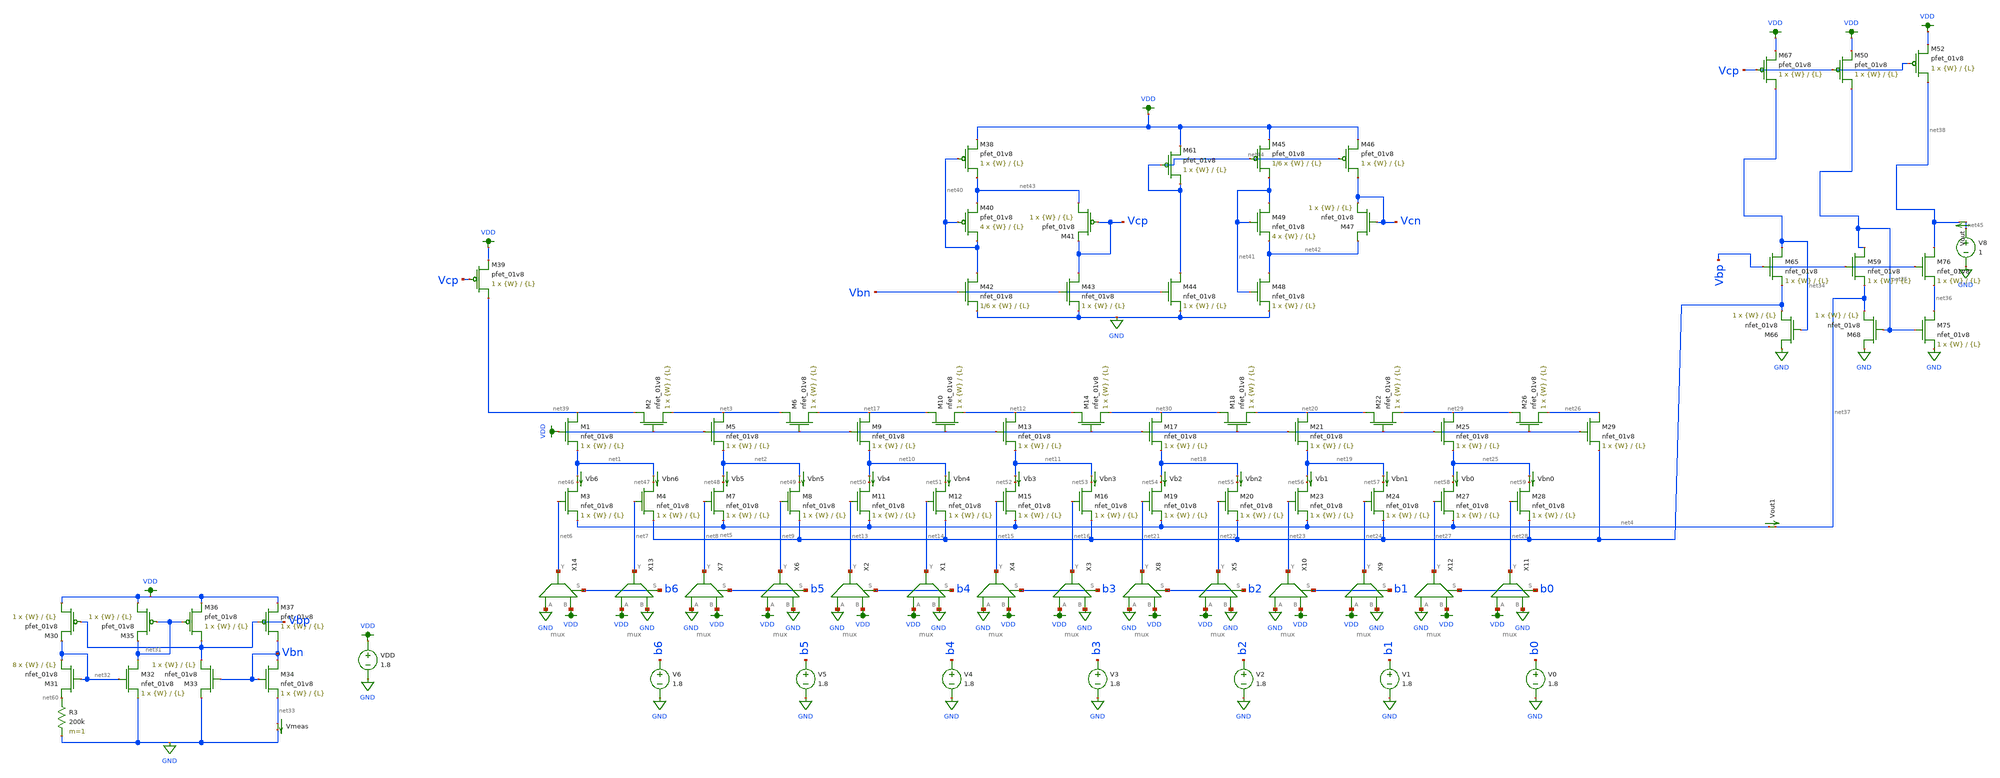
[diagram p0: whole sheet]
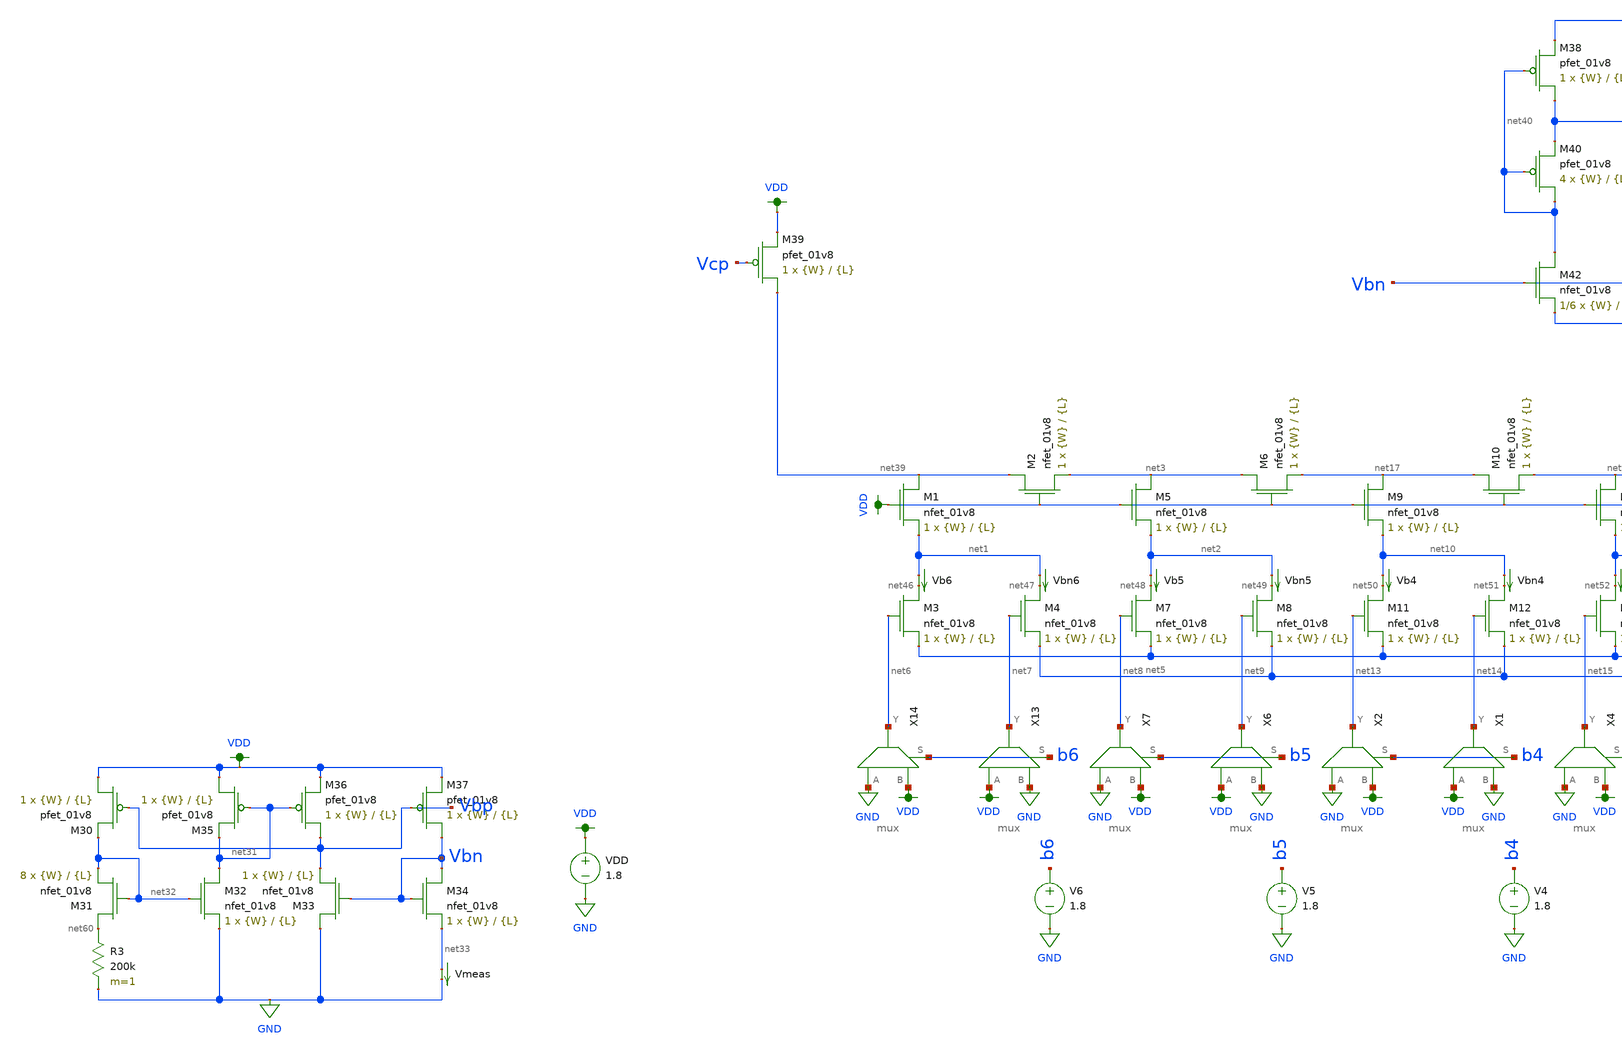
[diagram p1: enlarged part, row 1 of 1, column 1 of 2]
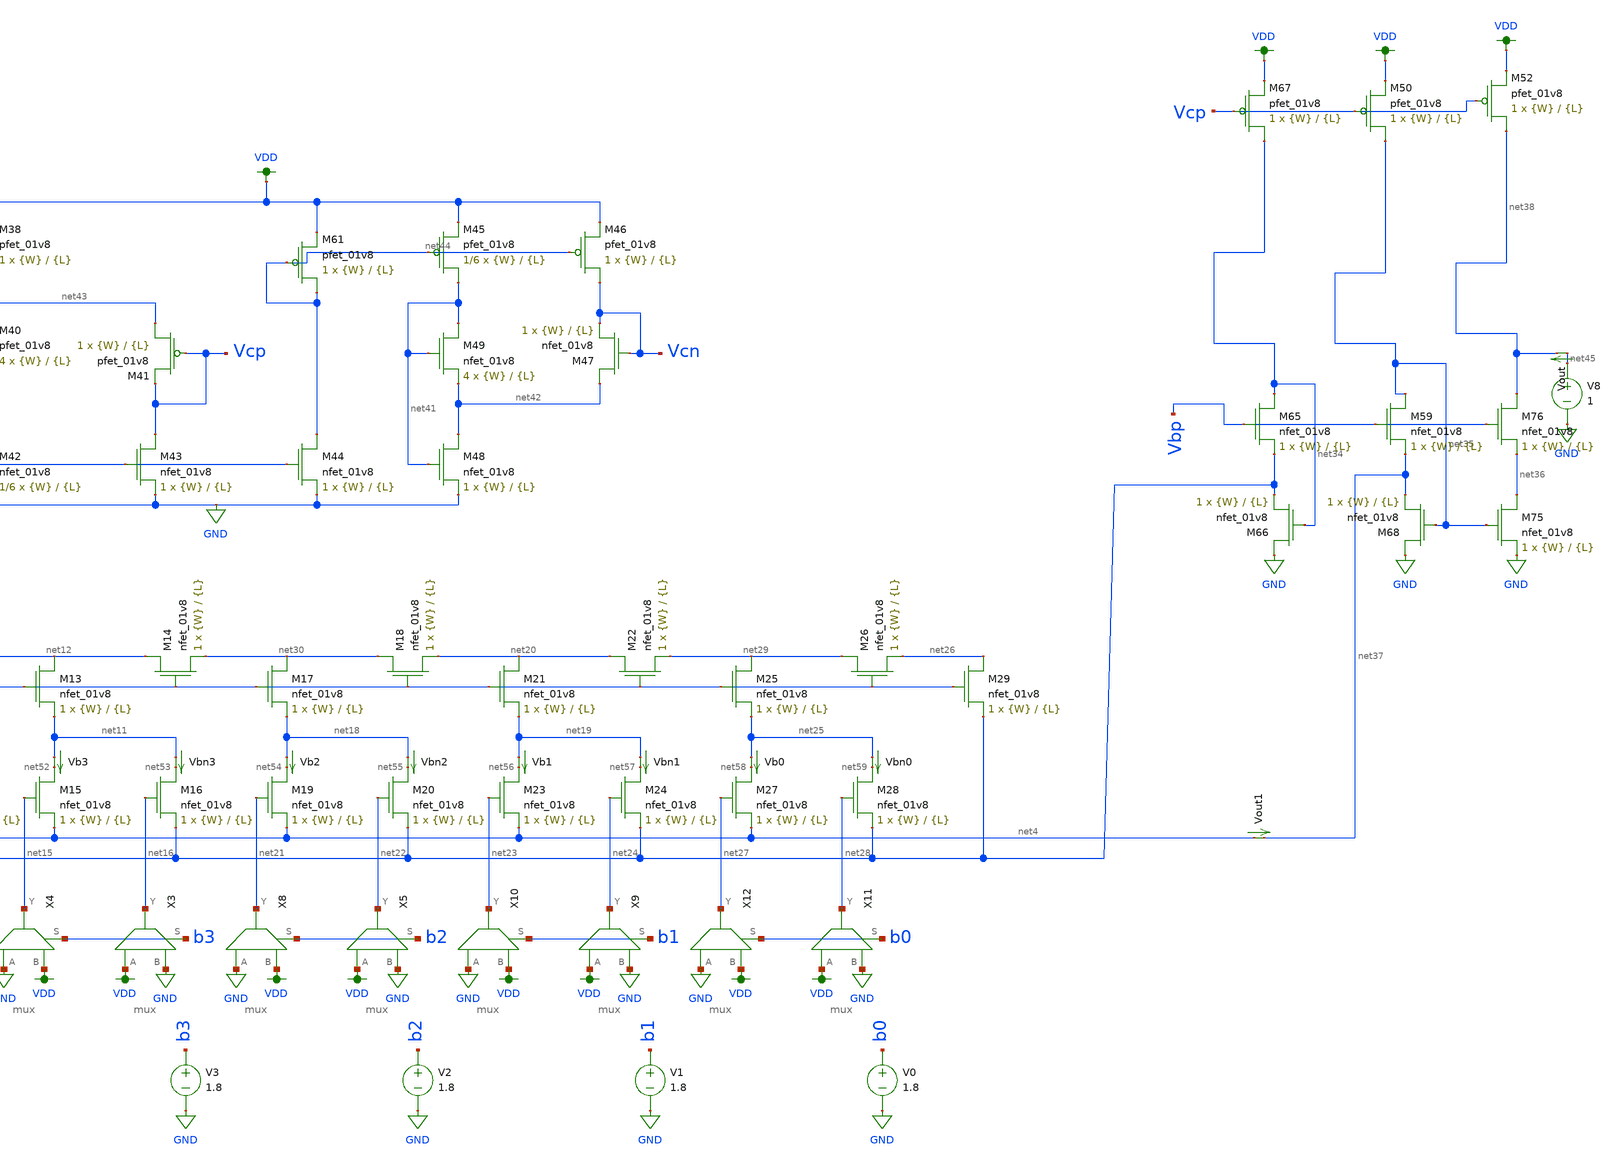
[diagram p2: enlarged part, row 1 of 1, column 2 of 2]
** sch_path: dac/schematics/misc/dac_from_paper_2.sch
**.subckt dac_from_paper_2
XM1 net39 VDD net1 GND sky130_fd_pr__nfet_01v8 L={L} W={W} nf=1 ad='int((nf+1)/2) * W/nf * 0.29' as='int((nf+2)/2) * W/nf * 0.29'
+ pd='2*int((nf+1)/2) * (W/nf + 0.29)' ps='2*int((nf+2)/2) * (W/nf + 0.29)' nrd='0.29 / W' nrs='0.29 / W'
+ sa=0 sb=0 sd=0 mult=1 m=1
XM2 net39 VDD net3 GND sky130_fd_pr__nfet_01v8 L={L} W={W} nf=1 ad='int((nf+1)/2) * W/nf * 0.29' as='int((nf+2)/2) * W/nf * 0.29'
+ pd='2*int((nf+1)/2) * (W/nf + 0.29)' ps='2*int((nf+2)/2) * (W/nf + 0.29)' nrd='0.29 / W' nrs='0.29 / W'
+ sa=0 sb=0 sd=0 mult=1 m=1
XM3 net46 net6 net4 GND sky130_fd_pr__nfet_01v8 L={L} W={W} nf=1 ad='int((nf+1)/2) * W/nf * 0.29' as='int((nf+2)/2) * W/nf * 0.29'
+ pd='2*int((nf+1)/2) * (W/nf + 0.29)' ps='2*int((nf+2)/2) * (W/nf + 0.29)' nrd='0.29 / W' nrs='0.29 / W'
+ sa=0 sb=0 sd=0 mult=1 m=1
XM4 net47 net7 net5 GND sky130_fd_pr__nfet_01v8 L={L} W={W} nf=1 ad='int((nf+1)/2) * W/nf * 0.29' as='int((nf+2)/2) * W/nf * 0.29'
+ pd='2*int((nf+1)/2) * (W/nf + 0.29)' ps='2*int((nf+2)/2) * (W/nf + 0.29)' nrd='0.29 / W' nrs='0.29 / W'
+ sa=0 sb=0 sd=0 mult=1 m=1
XM5 net3 VDD net2 GND sky130_fd_pr__nfet_01v8 L={L} W={W} nf=1 ad='int((nf+1)/2) * W/nf * 0.29' as='int((nf+2)/2) * W/nf * 0.29'
+ pd='2*int((nf+1)/2) * (W/nf + 0.29)' ps='2*int((nf+2)/2) * (W/nf + 0.29)' nrd='0.29 / W' nrs='0.29 / W'
+ sa=0 sb=0 sd=0 mult=1 m=1
XM6 net3 VDD net17 GND sky130_fd_pr__nfet_01v8 L={L} W={W} nf=1 ad='int((nf+1)/2) * W/nf * 0.29' as='int((nf+2)/2) * W/nf * 0.29'
+ pd='2*int((nf+1)/2) * (W/nf + 0.29)' ps='2*int((nf+2)/2) * (W/nf + 0.29)' nrd='0.29 / W' nrs='0.29 / W'
+ sa=0 sb=0 sd=0 mult=1 m=1
XM7 net48 net8 net4 GND sky130_fd_pr__nfet_01v8 L={L} W={W} nf=1 ad='int((nf+1)/2) * W/nf * 0.29' as='int((nf+2)/2) * W/nf * 0.29'
+ pd='2*int((nf+1)/2) * (W/nf + 0.29)' ps='2*int((nf+2)/2) * (W/nf + 0.29)' nrd='0.29 / W' nrs='0.29 / W'
+ sa=0 sb=0 sd=0 mult=1 m=1
XM8 net49 net9 net5 GND sky130_fd_pr__nfet_01v8 L={L} W={W} nf=1 ad='int((nf+1)/2) * W/nf * 0.29' as='int((nf+2)/2) * W/nf * 0.29'
+ pd='2*int((nf+1)/2) * (W/nf + 0.29)' ps='2*int((nf+2)/2) * (W/nf + 0.29)' nrd='0.29 / W' nrs='0.29 / W'
+ sa=0 sb=0 sd=0 mult=1 m=1
XM9 net17 VDD net10 GND sky130_fd_pr__nfet_01v8 L={L} W={W} nf=1 ad='int((nf+1)/2) * W/nf * 0.29' as='int((nf+2)/2) * W/nf * 0.29'
+ pd='2*int((nf+1)/2) * (W/nf + 0.29)' ps='2*int((nf+2)/2) * (W/nf + 0.29)' nrd='0.29 / W' nrs='0.29 / W'
+ sa=0 sb=0 sd=0 mult=1 m=1
XM10 net17 VDD net12 GND sky130_fd_pr__nfet_01v8 L={L} W={W} nf=1 ad='int((nf+1)/2) * W/nf * 0.29' as='int((nf+2)/2) * W/nf * 0.29'
+ pd='2*int((nf+1)/2) * (W/nf + 0.29)' ps='2*int((nf+2)/2) * (W/nf + 0.29)' nrd='0.29 / W' nrs='0.29 / W'
+ sa=0 sb=0 sd=0 mult=1 m=1
XM11 net50 net13 net4 GND sky130_fd_pr__nfet_01v8 L={L} W={W} nf=1 ad='int((nf+1)/2) * W/nf * 0.29' as='int((nf+2)/2) * W/nf * 0.29'
+ pd='2*int((nf+1)/2) * (W/nf + 0.29)' ps='2*int((nf+2)/2) * (W/nf + 0.29)' nrd='0.29 / W' nrs='0.29 / W'
+ sa=0 sb=0 sd=0 mult=1 m=1
XM12 net51 net14 net5 GND sky130_fd_pr__nfet_01v8 L={L} W={W} nf=1 ad='int((nf+1)/2) * W/nf * 0.29' as='int((nf+2)/2) * W/nf * 0.29'
+ pd='2*int((nf+1)/2) * (W/nf + 0.29)' ps='2*int((nf+2)/2) * (W/nf + 0.29)' nrd='0.29 / W' nrs='0.29 / W'
+ sa=0 sb=0 sd=0 mult=1 m=1
XM13 net12 VDD net11 GND sky130_fd_pr__nfet_01v8 L={L} W={W} nf=1 ad='int((nf+1)/2) * W/nf * 0.29' as='int((nf+2)/2) * W/nf * 0.29'
+ pd='2*int((nf+1)/2) * (W/nf + 0.29)' ps='2*int((nf+2)/2) * (W/nf + 0.29)' nrd='0.29 / W' nrs='0.29 / W'
+ sa=0 sb=0 sd=0 mult=1 m=1
XM14 net12 VDD net30 GND sky130_fd_pr__nfet_01v8 L={L} W={W} nf=1 ad='int((nf+1)/2) * W/nf * 0.29' as='int((nf+2)/2) * W/nf * 0.29'
+ pd='2*int((nf+1)/2) * (W/nf + 0.29)' ps='2*int((nf+2)/2) * (W/nf + 0.29)' nrd='0.29 / W' nrs='0.29 / W'
+ sa=0 sb=0 sd=0 mult=1 m=1
XM15 net52 net15 net4 GND sky130_fd_pr__nfet_01v8 L={L} W={W} nf=1 ad='int((nf+1)/2) * W/nf * 0.29' as='int((nf+2)/2) * W/nf * 0.29'
+ pd='2*int((nf+1)/2) * (W/nf + 0.29)' ps='2*int((nf+2)/2) * (W/nf + 0.29)' nrd='0.29 / W' nrs='0.29 / W'
+ sa=0 sb=0 sd=0 mult=1 m=1
XM16 net53 net16 net5 GND sky130_fd_pr__nfet_01v8 L={L} W={W} nf=1 ad='int((nf+1)/2) * W/nf * 0.29' as='int((nf+2)/2) * W/nf * 0.29'
+ pd='2*int((nf+1)/2) * (W/nf + 0.29)' ps='2*int((nf+2)/2) * (W/nf + 0.29)' nrd='0.29 / W' nrs='0.29 / W'
+ sa=0 sb=0 sd=0 mult=1 m=1
XM17 net30 VDD net18 GND sky130_fd_pr__nfet_01v8 L={L} W={W} nf=1 ad='int((nf+1)/2) * W/nf * 0.29' as='int((nf+2)/2) * W/nf * 0.29'
+ pd='2*int((nf+1)/2) * (W/nf + 0.29)' ps='2*int((nf+2)/2) * (W/nf + 0.29)' nrd='0.29 / W' nrs='0.29 / W'
+ sa=0 sb=0 sd=0 mult=1 m=1
XM18 net30 VDD net20 GND sky130_fd_pr__nfet_01v8 L={L} W={W} nf=1 ad='int((nf+1)/2) * W/nf * 0.29' as='int((nf+2)/2) * W/nf * 0.29'
+ pd='2*int((nf+1)/2) * (W/nf + 0.29)' ps='2*int((nf+2)/2) * (W/nf + 0.29)' nrd='0.29 / W' nrs='0.29 / W'
+ sa=0 sb=0 sd=0 mult=1 m=1
XM19 net54 net21 net4 GND sky130_fd_pr__nfet_01v8 L={L} W={W} nf=1 ad='int((nf+1)/2) * W/nf * 0.29' as='int((nf+2)/2) * W/nf * 0.29'
+ pd='2*int((nf+1)/2) * (W/nf + 0.29)' ps='2*int((nf+2)/2) * (W/nf + 0.29)' nrd='0.29 / W' nrs='0.29 / W'
+ sa=0 sb=0 sd=0 mult=1 m=1
XM20 net55 net22 net5 GND sky130_fd_pr__nfet_01v8 L={L} W={W} nf=1 ad='int((nf+1)/2) * W/nf * 0.29' as='int((nf+2)/2) * W/nf * 0.29'
+ pd='2*int((nf+1)/2) * (W/nf + 0.29)' ps='2*int((nf+2)/2) * (W/nf + 0.29)' nrd='0.29 / W' nrs='0.29 / W'
+ sa=0 sb=0 sd=0 mult=1 m=1
XM21 net20 VDD net19 GND sky130_fd_pr__nfet_01v8 L={L} W={W} nf=1 ad='int((nf+1)/2) * W/nf * 0.29' as='int((nf+2)/2) * W/nf * 0.29'
+ pd='2*int((nf+1)/2) * (W/nf + 0.29)' ps='2*int((nf+2)/2) * (W/nf + 0.29)' nrd='0.29 / W' nrs='0.29 / W'
+ sa=0 sb=0 sd=0 mult=1 m=1
XM22 net20 VDD net29 GND sky130_fd_pr__nfet_01v8 L={L} W={W} nf=1 ad='int((nf+1)/2) * W/nf * 0.29' as='int((nf+2)/2) * W/nf * 0.29'
+ pd='2*int((nf+1)/2) * (W/nf + 0.29)' ps='2*int((nf+2)/2) * (W/nf + 0.29)' nrd='0.29 / W' nrs='0.29 / W'
+ sa=0 sb=0 sd=0 mult=1 m=1
XM23 net56 net23 net4 GND sky130_fd_pr__nfet_01v8 L={L} W={W} nf=1 ad='int((nf+1)/2) * W/nf * 0.29' as='int((nf+2)/2) * W/nf * 0.29'
+ pd='2*int((nf+1)/2) * (W/nf + 0.29)' ps='2*int((nf+2)/2) * (W/nf + 0.29)' nrd='0.29 / W' nrs='0.29 / W'
+ sa=0 sb=0 sd=0 mult=1 m=1
XM24 net57 net24 net5 GND sky130_fd_pr__nfet_01v8 L={L} W={W} nf=1 ad='int((nf+1)/2) * W/nf * 0.29' as='int((nf+2)/2) * W/nf * 0.29'
+ pd='2*int((nf+1)/2) * (W/nf + 0.29)' ps='2*int((nf+2)/2) * (W/nf + 0.29)' nrd='0.29 / W' nrs='0.29 / W'
+ sa=0 sb=0 sd=0 mult=1 m=1
XM25 net29 VDD net25 GND sky130_fd_pr__nfet_01v8 L={L} W={W} nf=1 ad='int((nf+1)/2) * W/nf * 0.29' as='int((nf+2)/2) * W/nf * 0.29'
+ pd='2*int((nf+1)/2) * (W/nf + 0.29)' ps='2*int((nf+2)/2) * (W/nf + 0.29)' nrd='0.29 / W' nrs='0.29 / W'
+ sa=0 sb=0 sd=0 mult=1 m=1
XM26 net29 VDD net26 GND sky130_fd_pr__nfet_01v8 L={L} W={W} nf=1 ad='int((nf+1)/2) * W/nf * 0.29' as='int((nf+2)/2) * W/nf * 0.29'
+ pd='2*int((nf+1)/2) * (W/nf + 0.29)' ps='2*int((nf+2)/2) * (W/nf + 0.29)' nrd='0.29 / W' nrs='0.29 / W'
+ sa=0 sb=0 sd=0 mult=1 m=1
XM27 net58 net27 net4 GND sky130_fd_pr__nfet_01v8 L={L} W={W} nf=1 ad='int((nf+1)/2) * W/nf * 0.29' as='int((nf+2)/2) * W/nf * 0.29'
+ pd='2*int((nf+1)/2) * (W/nf + 0.29)' ps='2*int((nf+2)/2) * (W/nf + 0.29)' nrd='0.29 / W' nrs='0.29 / W'
+ sa=0 sb=0 sd=0 mult=1 m=1
XM28 net59 net28 net5 GND sky130_fd_pr__nfet_01v8 L={L} W={W} nf=1 ad='int((nf+1)/2) * W/nf * 0.29' as='int((nf+2)/2) * W/nf * 0.29'
+ pd='2*int((nf+1)/2) * (W/nf + 0.29)' ps='2*int((nf+2)/2) * (W/nf + 0.29)' nrd='0.29 / W' nrs='0.29 / W'
+ sa=0 sb=0 sd=0 mult=1 m=1
XM29 net26 VDD net5 GND sky130_fd_pr__nfet_01v8 L={L} W={W} nf=1 ad='int((nf+1)/2) * W/nf * 0.29' as='int((nf+2)/2) * W/nf * 0.29'
+ pd='2*int((nf+1)/2) * (W/nf + 0.29)' ps='2*int((nf+2)/2) * (W/nf + 0.29)' nrd='0.29 / W' nrs='0.29 / W'
+ sa=0 sb=0 sd=0 mult=1 m=1
Vb0 net25 net58 0
.save i(vb0)
Vbn0 net25 net59 0
.save i(vbn0)
Vb5 net2 net48 0
.save i(vb5)
Vb6 net1 net46 0
.save i(vb6)
Vb1 net19 net56 0
.save i(vb1)
Vb2 net18 net54 0
.save i(vb2)
Vb3 net11 net52 0
.save i(vb3)
Vb4 net10 net50 0
.save i(vb4)
Vbn1 net19 net57 0
.save i(vbn1)
Vbn2 net18 net55 0
.save i(vbn2)
Vbn3 net11 net53 0
.save i(vbn3)
Vbn4 net10 net51 0
.save i(vbn4)
Vbn5 net2 net49 0
.save i(vbn5)
Vbn6 net1 net47 0
.save i(vbn6)
V0 b0 GND 1.8
V1 b1 GND 1.8
V2 b2 GND 1.8
V3 b3 GND 1.8
V4 b4 GND 1.8
V5 b5 GND 1.8
V6 b6 GND 1.8
XM30 VDD Vbp net32 VDD sky130_fd_pr__pfet_01v8 L={L} W={W} nf=1 ad='int((nf+1)/2) * W/nf * 0.29' as='int((nf+2)/2) * W/nf * 0.29'
+ pd='2*int((nf+1)/2) * (W/nf + 0.29)' ps='2*int((nf+2)/2) * (W/nf + 0.29)' nrd='0.29 / W' nrs='0.29 / W'
+ sa=0 sb=0 sd=0 mult=1 m=1
XM31 net60 net32 net32 GND sky130_fd_pr__nfet_01v8 L={L} W={W} nf=1 ad='int((nf+1)/2) * W/nf * 0.29'
+ as='int((nf+2)/2) * W/nf * 0.29' pd='2*int((nf+1)/2) * (W/nf + 0.29)' ps='2*int((nf+2)/2) * (W/nf + 0.29)'
+ nrd='0.29 / W' nrs='0.29 / W' sa=0 sb=0 sd=0 mult=8 m=8
R3 net60 GND 200k m=1
XM32 net31 net32 GND GND sky130_fd_pr__nfet_01v8 L={L} W={W} nf=1 ad='int((nf+1)/2) * W/nf * 0.29' as='int((nf+2)/2) * W/nf * 0.29'
+ pd='2*int((nf+1)/2) * (W/nf + 0.29)' ps='2*int((nf+2)/2) * (W/nf + 0.29)' nrd='0.29 / W' nrs='0.29 / W'
+ sa=0 sb=0 sd=0 mult=1 m=1
XM33 GND Vbn Vbp GND sky130_fd_pr__nfet_01v8 L={L} W={W} nf=1 ad='int((nf+1)/2) * W/nf * 0.29' as='int((nf+2)/2) * W/nf * 0.29'
+ pd='2*int((nf+1)/2) * (W/nf + 0.29)' ps='2*int((nf+2)/2) * (W/nf + 0.29)' nrd='0.29 / W' nrs='0.29 / W'
+ sa=0 sb=0 sd=0 mult=1 m=1
XM34 Vbn Vbn net33 GND sky130_fd_pr__nfet_01v8 L={L} W={W} nf=1 ad='int((nf+1)/2) * W/nf * 0.29' as='int((nf+2)/2) * W/nf * 0.29'
+ pd='2*int((nf+1)/2) * (W/nf + 0.29)' ps='2*int((nf+2)/2) * (W/nf + 0.29)' nrd='0.29 / W' nrs='0.29 / W'
+ sa=0 sb=0 sd=0 mult=1 m=1
XM35 VDD net31 net31 VDD sky130_fd_pr__pfet_01v8 L={L} W={W} nf=1 ad='int((nf+1)/2) * W/nf * 0.29' as='int((nf+2)/2) * W/nf * 0.29'
+ pd='2*int((nf+1)/2) * (W/nf + 0.29)' ps='2*int((nf+2)/2) * (W/nf + 0.29)' nrd='0.29 / W' nrs='0.29 / W'
+ sa=0 sb=0 sd=0 mult=1 m=1
XM36 Vbp net31 VDD VDD sky130_fd_pr__pfet_01v8 L={L} W={W} nf=1 ad='int((nf+1)/2) * W/nf * 0.29' as='int((nf+2)/2) * W/nf * 0.29'
+ pd='2*int((nf+1)/2) * (W/nf + 0.29)' ps='2*int((nf+2)/2) * (W/nf + 0.29)' nrd='0.29 / W' nrs='0.29 / W'
+ sa=0 sb=0 sd=0 mult=1 m=1
XM37 Vbn Vbp VDD VDD sky130_fd_pr__pfet_01v8 L={L} W={W} nf=1 ad='int((nf+1)/2) * W/nf * 0.29' as='int((nf+2)/2) * W/nf * 0.29'
+ pd='2*int((nf+1)/2) * (W/nf + 0.29)' ps='2*int((nf+2)/2) * (W/nf + 0.29)' nrd='0.29 / W' nrs='0.29 / W'
+ sa=0 sb=0 sd=0 mult=1 m=1
VDD VDD GND 1.8
Vmeas net33 GND 0
.save i(vmeas)
X13 VDD GND net7 b6 mux
X14 GND VDD net6 b6 mux
X6 VDD GND net9 b5 mux
X7 GND VDD net8 b5 mux
X1 VDD GND net14 b4 mux
X2 GND VDD net13 b4 mux
X3 VDD GND net16 b3 mux
X4 GND VDD net15 b3 mux
X5 VDD GND net22 b2 mux
X8 GND VDD net21 b2 mux
X9 VDD GND net24 b1 mux
X10 GND VDD net23 b1 mux
X11 VDD GND net28 b0 mux
X12 GND VDD net27 b0 mux
XM65 net34 Vbp net5 GND sky130_fd_pr__nfet_01v8 L={L} W={W} nf=1 ad='int((nf+1)/2) * W/nf * 0.29' as='int((nf+2)/2) * W/nf * 0.29'
+ pd='2*int((nf+1)/2) * (W/nf + 0.29)' ps='2*int((nf+2)/2) * (W/nf + 0.29)' nrd='0.29 / W' nrs='0.29 / W'
+ sa=0 sb=0 sd=0 mult=1 m=1
XM66 GND net34 net5 GND sky130_fd_pr__nfet_01v8 L={L} W={W} nf=1 ad='int((nf+1)/2) * W/nf * 0.29' as='int((nf+2)/2) * W/nf * 0.29'
+ pd='2*int((nf+1)/2) * (W/nf + 0.29)' ps='2*int((nf+2)/2) * (W/nf + 0.29)' nrd='0.29 / W' nrs='0.29 / W'
+ sa=0 sb=0 sd=0 mult=1 m=1
XM59 net35 Vbp net37 GND sky130_fd_pr__nfet_01v8 L={L} W={W} nf=1 ad='int((nf+1)/2) * W/nf * 0.29' as='int((nf+2)/2) * W/nf * 0.29'
+ pd='2*int((nf+1)/2) * (W/nf + 0.29)' ps='2*int((nf+2)/2) * (W/nf + 0.29)' nrd='0.29 / W' nrs='0.29 / W'
+ sa=0 sb=0 sd=0 mult=1 m=1
XM68 GND net35 net37 GND sky130_fd_pr__nfet_01v8 L={L} W={W} nf=1 ad='int((nf+1)/2) * W/nf * 0.29' as='int((nf+2)/2) * W/nf * 0.29'
+ pd='2*int((nf+1)/2) * (W/nf + 0.29)' ps='2*int((nf+2)/2) * (W/nf + 0.29)' nrd='0.29 / W' nrs='0.29 / W'
+ sa=0 sb=0 sd=0 mult=1 m=1
XM75 net36 net35 GND GND sky130_fd_pr__nfet_01v8 L={L} W={W} nf=1 ad='int((nf+1)/2) * W/nf * 0.29' as='int((nf+2)/2) * W/nf * 0.29'
+ pd='2*int((nf+1)/2) * (W/nf + 0.29)' ps='2*int((nf+2)/2) * (W/nf + 0.29)' nrd='0.29 / W' nrs='0.29 / W'
+ sa=0 sb=0 sd=0 mult=1 m=1
XM76 net38 Vbp net36 GND sky130_fd_pr__nfet_01v8 L={L} W={W} nf=1 ad='int((nf+1)/2) * W/nf * 0.29' as='int((nf+2)/2) * W/nf * 0.29'
+ pd='2*int((nf+1)/2) * (W/nf + 0.29)' ps='2*int((nf+2)/2) * (W/nf + 0.29)' nrd='0.29 / W' nrs='0.29 / W'
+ sa=0 sb=0 sd=0 mult=1 m=1
Vout net45 net38 0
.save i(vout)
XM67 net34 Vcp VDD VDD sky130_fd_pr__pfet_01v8 L={L} W={W} nf=6 ad='int((nf+1)/2) * W/nf * 0.29' as='int((nf+2)/2) * W/nf * 0.29'
+ pd='2*int((nf+1)/2) * (W/nf + 0.29)' ps='2*int((nf+2)/2) * (W/nf + 0.29)' nrd='0.29 / W' nrs='0.29 / W'
+ sa=0 sb=0 sd=0 mult=1 m=1
XM50 net35 Vcp VDD VDD sky130_fd_pr__pfet_01v8 L={L} W={W} nf=6 ad='int((nf+1)/2) * W/nf * 0.29' as='int((nf+2)/2) * W/nf * 0.29'
+ pd='2*int((nf+1)/2) * (W/nf + 0.29)' ps='2*int((nf+2)/2) * (W/nf + 0.29)' nrd='0.29 / W' nrs='0.29 / W'
+ sa=0 sb=0 sd=0 mult=1 m=1
XM52 net38 Vcp VDD VDD sky130_fd_pr__pfet_01v8 L={L} W={W} nf=6 ad='int((nf+1)/2) * W/nf * 0.29' as='int((nf+2)/2) * W/nf * 0.29'
+ pd='2*int((nf+1)/2) * (W/nf + 0.29)' ps='2*int((nf+2)/2) * (W/nf + 0.29)' nrd='0.29 / W' nrs='0.29 / W'
+ sa=0 sb=0 sd=0 mult=1 m=1
Vout1 net4 net37 0
.save i(vout1)
XM39 net39 Vcp VDD VDD sky130_fd_pr__pfet_01v8 L={L} W={W} nf=1 ad='int((nf+1)/2) * W/nf * 0.29' as='int((nf+2)/2) * W/nf * 0.29'
+ pd='2*int((nf+1)/2) * (W/nf + 0.29)' ps='2*int((nf+2)/2) * (W/nf + 0.29)' nrd='0.29 / W' nrs='0.29 / W'
+ sa=0 sb=0 sd=0 mult=1 m=1
XM38 net43 net40 VDD VDD sky130_fd_pr__pfet_01v8 L={L} W={W} nf=1 ad='int((nf+1)/2) * W/nf * 0.29' as='int((nf+2)/2) * W/nf * 0.29'
+ pd='2*int((nf+1)/2) * (W/nf + 0.29)' ps='2*int((nf+2)/2) * (W/nf + 0.29)' nrd='0.29 / W' nrs='0.29 / W'
+ sa=0 sb=0 sd=0 mult=1 m=1
XM40 net40 net40 net43 VDD sky130_fd_pr__pfet_01v8 L={L} W={W} nf=1 ad='int((nf+1)/2) * W/nf * 0.29'
+ as='int((nf+2)/2) * W/nf * 0.29' pd='2*int((nf+1)/2) * (W/nf + 0.29)' ps='2*int((nf+2)/2) * (W/nf + 0.29)'
+ nrd='0.29 / W' nrs='0.29 / W' sa=0 sb=0 sd=0 mult=4 m=4
XM41 net43 Vcp Vcp VDD sky130_fd_pr__pfet_01v8 L={L} W={W} nf=1 ad='int((nf+1)/2) * W/nf * 0.29' as='int((nf+2)/2) * W/nf * 0.29'
+ pd='2*int((nf+1)/2) * (W/nf + 0.29)' ps='2*int((nf+2)/2) * (W/nf + 0.29)' nrd='0.29 / W' nrs='0.29 / W'
+ sa=0 sb=0 sd=0 mult=1 m=1
XM42 net40 Vbn GND GND sky130_fd_pr__nfet_01v8 L={L} W={W} nf=1 ad='int((nf+1)/2) * W/nf * 0.29' as='int((nf+2)/2) * W/nf * 0.29'
+ pd='2*int((nf+1)/2) * (W/nf + 0.29)' ps='2*int((nf+2)/2) * (W/nf + 0.29)' nrd='0.29 / W' nrs='0.29 / W'
+ sa=0 sb=0 sd=0 mult=1/6 m=1/6
XM43 Vcp Vbn GND GND sky130_fd_pr__nfet_01v8 L={L} W={W} nf=1 ad='int((nf+1)/2) * W/nf * 0.29' as='int((nf+2)/2) * W/nf * 0.29'
+ pd='2*int((nf+1)/2) * (W/nf + 0.29)' ps='2*int((nf+2)/2) * (W/nf + 0.29)' nrd='0.29 / W' nrs='0.29 / W'
+ sa=0 sb=0 sd=0 mult=1 m=1
XM44 net44 Vbn GND GND sky130_fd_pr__nfet_01v8 L={L} W={W} nf=1 ad='int((nf+1)/2) * W/nf * 0.29' as='int((nf+2)/2) * W/nf * 0.29'
+ pd='2*int((nf+1)/2) * (W/nf + 0.29)' ps='2*int((nf+2)/2) * (W/nf + 0.29)' nrd='0.29 / W' nrs='0.29 / W'
+ sa=0 sb=0 sd=0 mult=1 m=1
XM45 net41 net44 VDD VDD sky130_fd_pr__pfet_01v8 L={L} W={W} nf=1 ad='int((nf+1)/2) * W/nf * 0.29' as='int((nf+2)/2) * W/nf * 0.29'
+ pd='2*int((nf+1)/2) * (W/nf + 0.29)' ps='2*int((nf+2)/2) * (W/nf + 0.29)' nrd='0.29 / W' nrs='0.29 / W'
+ sa=0 sb=0 sd=0 mult=1/6 m=1/6
XM46 Vcn net44 VDD VDD sky130_fd_pr__pfet_01v8 L={L} W={W} nf=1 ad='int((nf+1)/2) * W/nf * 0.29' as='int((nf+2)/2) * W/nf * 0.29'
+ pd='2*int((nf+1)/2) * (W/nf + 0.29)' ps='2*int((nf+2)/2) * (W/nf + 0.29)' nrd='0.29 / W' nrs='0.29 / W'
+ sa=0 sb=0 sd=0 mult=1 m=1
XM47 net42 Vcn Vcn GND sky130_fd_pr__nfet_01v8 L={L} W={W} nf=1 ad='int((nf+1)/2) * W/nf * 0.29' as='int((nf+2)/2) * W/nf * 0.29'
+ pd='2*int((nf+1)/2) * (W/nf + 0.29)' ps='2*int((nf+2)/2) * (W/nf + 0.29)' nrd='0.29 / W' nrs='0.29 / W'
+ sa=0 sb=0 sd=0 mult=1 m=1
XM48 net42 net41 GND GND sky130_fd_pr__nfet_01v8 L={L} W={W} nf=1 ad='int((nf+1)/2) * W/nf * 0.29' as='int((nf+2)/2) * W/nf * 0.29'
+ pd='2*int((nf+1)/2) * (W/nf + 0.29)' ps='2*int((nf+2)/2) * (W/nf + 0.29)' nrd='0.29 / W' nrs='0.29 / W'
+ sa=0 sb=0 sd=0 mult=1 m=1
XM49 net41 net41 net42 GND sky130_fd_pr__nfet_01v8 L={L} W={W} nf=1 ad='int((nf+1)/2) * W/nf * 0.29'
+ as='int((nf+2)/2) * W/nf * 0.29' pd='2*int((nf+1)/2) * (W/nf + 0.29)' ps='2*int((nf+2)/2) * (W/nf + 0.29)'
+ nrd='0.29 / W' nrs='0.29 / W' sa=0 sb=0 sd=0 mult=4 m=4
XM61 net44 net44 VDD VDD sky130_fd_pr__pfet_01v8 L={L} W={W} nf=1 ad='int((nf+1)/2) * W/nf * 0.29' as='int((nf+2)/2) * W/nf * 0.29'
+ pd='2*int((nf+1)/2) * (W/nf + 0.29)' ps='2*int((nf+2)/2) * (W/nf + 0.29)' nrd='0.29 / W' nrs='0.29 / W'
+ sa=0 sb=0 sd=0 mult=1 m=1
V8 net45 GND 1
**** begin user architecture code

.option wnflag=1
.param MC_SWITCH=0.0
.lib ~/skywater/skywater-pdk/libraries/sky130_fd_pr_ngspice/latest/models/sky130.lib.spice tt


.param W=64
.param L=8
.control
set wr_vecnames
set wr_singlescale
let code = 0
  while code < 128
    if code eq 0
      let b0 = 0
    else
      let b0 = code % 2
    end
    if floor(code / 2) eq 0
      let b1 = 0
    else
      let b1 = floor(code / 2) % 2
    end
    if floor(code / 4) eq 0
      let b2 = 0
    else
      let b2 = floor(code / 4) % 2
    end
    if floor(code / 8) eq 0
      let b3 = 0
    else
      let b3 = floor(code / 8) % 2
    end
    if floor(code / 16) eq 0
      let b4 = 0
    else
      let b4 = floor(code / 16) % 2
    end
    if floor(code / 32) eq 0
      let b5 = 0
    else
      let b5 = floor(code / 32) % 2
    end
    if floor(code / 64) eq 0
      let b6 = 0
    else
      let b6 = floor(code / 64) % 2
    end
    alter v0 $&b0
    alter v1 $&b1
    alter v2 $&b2
    alter v3 $&b3
    alter v4 $&b4
    alter v5 $&b5
    alter v6 $&b6
    save all
    op
    wrdata ~/Documents/current-output-dac-vlsi/simulations/dac_paper_sim.txt i(Vmeas) i(vb0) i(vb1)
+ i(vb2) i(vb3) i(vb4) i(vb5) i(vb6) i(Vout) i(Vout1)
    if code eq 0
      set appendwrite
      set wr_vecnames = FALSE
    end
    let code = code + 1
  end
.endc

**** end user architecture code
**.ends

* expanding   symbol:  /home/madvlsi/Documents/current-output-dac-vlsi/schematics/mux.sym # of
*+ pins=4
** sym_path: dac/schematics/mux.sym
** sch_path: dac/schematics/mux.sch
.subckt mux A B Y S
*.ipin A
*.ipin B
*.ipin S
*.opin Y
XM1 A S Y VDD sky130_fd_pr__pfet_01v8 L=0.15 W=1 nf=1 ad='int((nf+1)/2) * W/nf * 0.29' as='int((nf+2)/2) * W/nf * 0.29'
+ pd='2*int((nf+1)/2) * (W/nf + 0.29)' ps='2*int((nf+2)/2) * (W/nf + 0.29)' nrd='0.29 / W' nrs='0.29 / W'
+ sa=0 sb=0 sd=0 mult=1 m=1
XM3 net1 S VDD VDD sky130_fd_pr__pfet_01v8 L=0.15 W=1 nf=1 ad='int((nf+1)/2) * W/nf * 0.29' as='int((nf+2)/2) * W/nf * 0.29'
+ pd='2*int((nf+1)/2) * (W/nf + 0.29)' ps='2*int((nf+2)/2) * (W/nf + 0.29)' nrd='0.29 / W' nrs='0.29 / W'
+ sa=0 sb=0 sd=0 mult=1 m=1
XM4 net1 S GND GND sky130_fd_pr__nfet_01v8 L=0.15 W=1 nf=1 ad='int((nf+1)/2) * W/nf * 0.29' as='int((nf+2)/2) * W/nf * 0.29'
+ pd='2*int((nf+1)/2) * (W/nf + 0.29)' ps='2*int((nf+2)/2) * (W/nf + 0.29)' nrd='0.29 / W' nrs='0.29 / W'
+ sa=0 sb=0 sd=0 mult=1 m=1
XM5 A net1 Y GND sky130_fd_pr__nfet_01v8 L=0.15 W=1 nf=1 ad='int((nf+1)/2) * W/nf * 0.29' as='int((nf+2)/2) * W/nf * 0.29'
+ pd='2*int((nf+1)/2) * (W/nf + 0.29)' ps='2*int((nf+2)/2) * (W/nf + 0.29)' nrd='0.29 / W' nrs='0.29 / W'
+ sa=0 sb=0 sd=0 mult=1 m=1
XM2 B net1 Y VDD sky130_fd_pr__pfet_01v8 L=0.15 W=1 nf=1 ad='int((nf+1)/2) * W/nf * 0.29' as='int((nf+2)/2) * W/nf * 0.29'
+ pd='2*int((nf+1)/2) * (W/nf + 0.29)' ps='2*int((nf+2)/2) * (W/nf + 0.29)' nrd='0.29 / W' nrs='0.29 / W'
+ sa=0 sb=0 sd=0 mult=1 m=1
XM6 B S Y GND sky130_fd_pr__nfet_01v8 L=0.15 W=1 nf=1 ad='int((nf+1)/2) * W/nf * 0.29' as='int((nf+2)/2) * W/nf * 0.29'
+ pd='2*int((nf+1)/2) * (W/nf + 0.29)' ps='2*int((nf+2)/2) * (W/nf + 0.29)' nrd='0.29 / W' nrs='0.29 / W'
+ sa=0 sb=0 sd=0 mult=1 m=1
.ends

.GLOBAL GND
.GLOBAL VDD
.end
